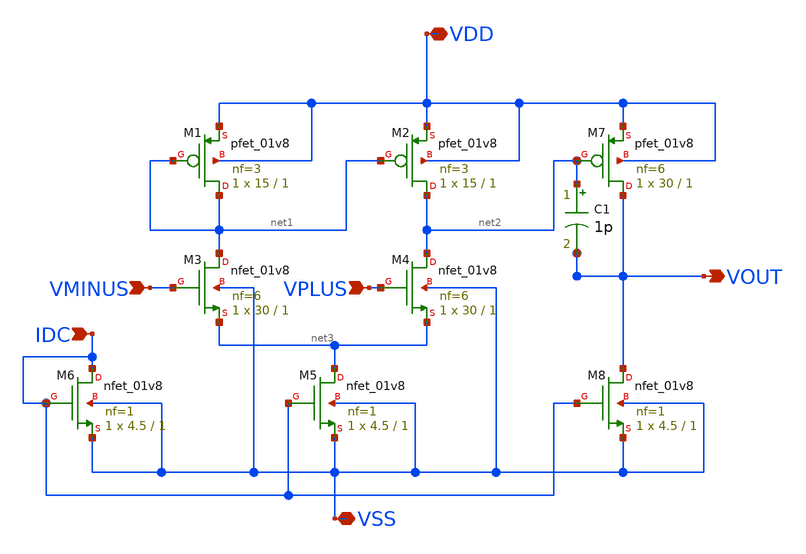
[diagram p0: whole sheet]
** sch_path: coba1_skematik.sch
**.subckt coba1_skematik VPLUS VMINUS IDC VOUT VDD VSS
*.ipin VPLUS
*.ipin VMINUS
*.ipin IDC
*.opin VOUT
*.iopin VDD
*.iopin VSS
XM1 net1 net1 VDD VDD sky130_fd_pr__pfet_01v8 L=1 W=15 nf=3 ad='int((3 + 1)/2) * 15 / 3 * 0.29' as='int((3 + 2)/2) * 15 / 3 * 0.29'
+ pd='2*int((3 + 1)/2) * (15 / 3 + 0.29)' ps='2*int((3 + 2)/2) * (15 / 3 + 0.29)' nrd='0.29 / 15 ' nrs='0.29 / 15 '
+ sa=0 sb=0 sd=0 mult=1 m=1
XM2 net2 net1 VDD VDD sky130_fd_pr__pfet_01v8 L=1 W=15 nf=3 ad='int((3 + 1)/2) * 15 / 3 * 0.29' as='int((3 + 2)/2) * 15 / 3 * 0.29'
+ pd='2*int((3 + 1)/2) * (15 / 3 + 0.29)' ps='2*int((3 + 2)/2) * (15 / 3 + 0.29)' nrd='0.29 / 15 ' nrs='0.29 / 15 '
+ sa=0 sb=0 sd=0 mult=1 m=1
XM3 net1 VMINUS net3 VSS sky130_fd_pr__nfet_01v8 L=1 W=30 nf=6 ad='int((6 + 1)/2) * 30 / 6 * 0.29' as='int((6 + 2)/2) * 30 / 6 * 0.29'
+ pd='2*int((6 + 1)/2) * (30 / 6 + 0.29)' ps='2*int((6 + 2)/2) * (30 / 6 + 0.29)' nrd='0.29 / 30 ' nrs='0.29 / 30 '
+ sa=0 sb=0 sd=0 mult=1 m=1
XM4 net2 VPLUS net3 VSS sky130_fd_pr__nfet_01v8 L=1 W=30 nf=6 ad='int((6 + 1)/2) * 30 / 6 * 0.29' as='int((6 + 2)/2) * 30 / 6 * 0.29'
+ pd='2*int((6 + 1)/2) * (30 / 6 + 0.29)' ps='2*int((6 + 2)/2) * (30 / 6 + 0.29)' nrd='0.29 / 30 ' nrs='0.29 / 30 '
+ sa=0 sb=0 sd=0 mult=1 m=1
XM5 net3 IDC VSS VSS sky130_fd_pr__nfet_01v8 L=1 W=4.5 nf=1 ad='int((1 + 1)/2) * 4.5 / 1 * 0.29' as='int((1 + 2)/2) * 4.5 / 1 * 0.29'
+ pd='2*int((1 + 1)/2) * (4.5 / 1 + 0.29)' ps='2*int((1 + 2)/2) * (4.5 / 1 + 0.29)' nrd='0.29 / 4.5 ' nrs='0.29 / 4.5 '
+ sa=0 sb=0 sd=0 mult=1 m=1
XM6 IDC IDC VSS VSS sky130_fd_pr__nfet_01v8 L=1 W=4.5 nf=1 ad='int((1 + 1)/2) * 4.5 / 1 * 0.29' as='int((1 + 2)/2) * 4.5 / 1 * 0.29'
+ pd='2*int((1 + 1)/2) * (4.5 / 1 + 0.29)' ps='2*int((1 + 2)/2) * (4.5 / 1 + 0.29)' nrd='0.29 / 4.5 ' nrs='0.29 / 4.5 '
+ sa=0 sb=0 sd=0 mult=1 m=1
XM7 VOUT net2 VDD VDD sky130_fd_pr__pfet_01v8 L=1 W=30 nf=6 ad='int((6 + 1)/2) * 30 / 6 * 0.29' as='int((6 + 2)/2) * 30 / 6 * 0.29'
+ pd='2*int((6 + 1)/2) * (30 / 6 + 0.29)' ps='2*int((6 + 2)/2) * (30 / 6 + 0.29)' nrd='0.29 / 30 ' nrs='0.29 / 30 '
+ sa=0 sb=0 sd=0 mult=1 m=1
XM8 VOUT IDC VSS VSS sky130_fd_pr__nfet_01v8 L=1 W=4.5 nf=1 ad='int((1 + 1)/2) * 4.5 / 1 * 0.29' as='int((1 + 2)/2) * 4.5 / 1 * 0.29'
+ pd='2*int((1 + 1)/2) * (4.5 / 1 + 0.29)' ps='2*int((1 + 2)/2) * (4.5 / 1 + 0.29)' nrd='0.29 / 4.5 ' nrs='0.29 / 4.5 '
+ sa=0 sb=0 sd=0 mult=1 m=1
C1 net2 VOUT 1p m=1
**.ends
.end
